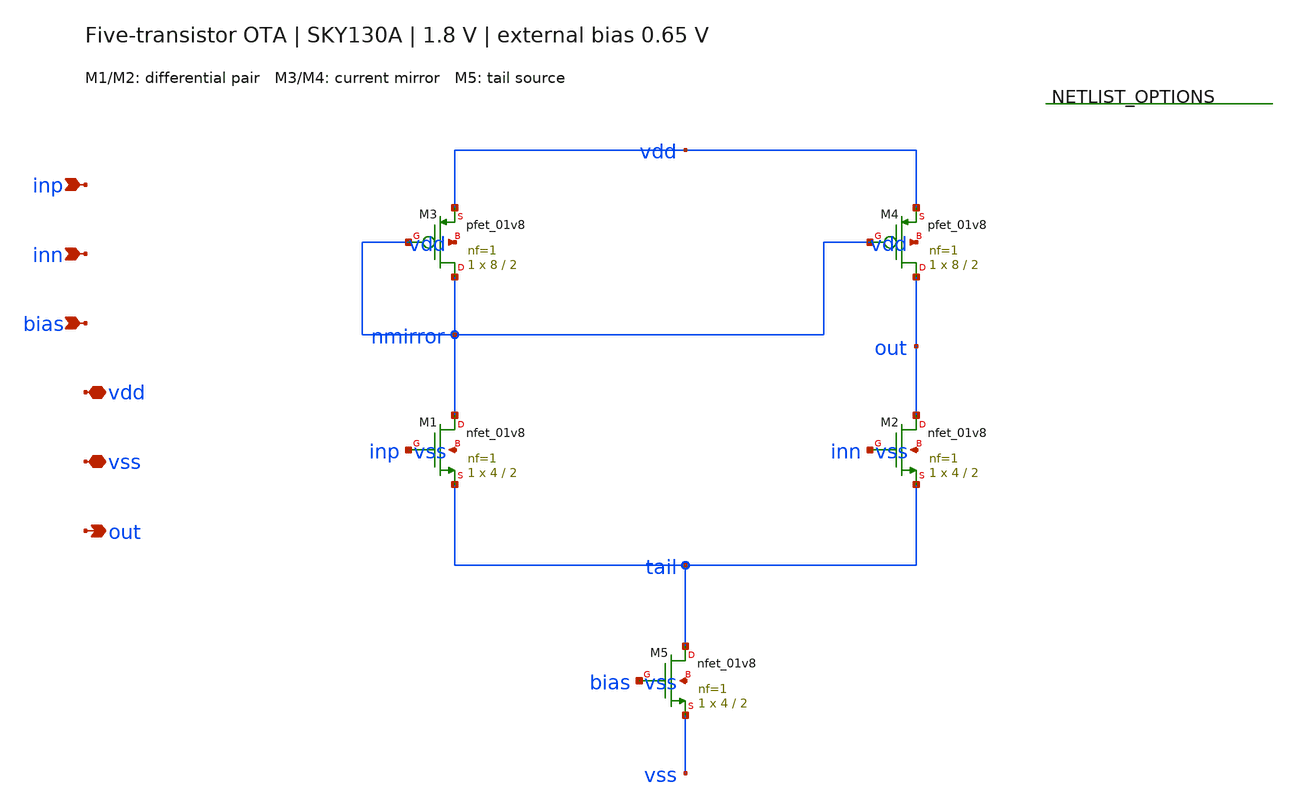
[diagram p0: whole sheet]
** sch_path: examples/ota5/schematics/ota5.sch
**.subckt ota5 inp inn bias vdd vss out
*.ipin inp
*.ipin inn
*.ipin bias
*.iopin vdd
*.iopin vss
*.opin out
XM1 nmirror inp tail vss sky130_fd_pr__nfet_01v8 L=2 W=4 nf=1 ad='int((1 + 1)/2) * 4 / 1 * 0.29' as='int((1 + 2)/2) * 4 / 1 * 0.29'
+ pd='2*int((1 + 1)/2) * (4 / 1 + 0.29)' ps='2*int((1 + 2)/2) * (4 / 1 + 0.29)' nrd='0.29 / 4 ' nrs='0.29 / 4 '
+ sa=0 sb=0 sd=0 mult=1 m=1
XM2 out inn tail vss sky130_fd_pr__nfet_01v8 L=2 W=4 nf=1 ad='int((1 + 1)/2) * 4 / 1 * 0.29' as='int((1 + 2)/2) * 4 / 1 * 0.29'
+ pd='2*int((1 + 1)/2) * (4 / 1 + 0.29)' ps='2*int((1 + 2)/2) * (4 / 1 + 0.29)' nrd='0.29 / 4 ' nrs='0.29 / 4 '
+ sa=0 sb=0 sd=0 mult=1 m=1
XM3 nmirror nmirror vdd vdd sky130_fd_pr__pfet_01v8 L=2 W=8 nf=1 ad='int((1 + 1)/2) * 8 / 1 * 0.29' as='int((1 + 2)/2) * 8 / 1 * 0.29'
+ pd='2*int((1 + 1)/2) * (8 / 1 + 0.29)' ps='2*int((1 + 2)/2) * (8 / 1 + 0.29)' nrd='0.29 / 8 ' nrs='0.29 / 8 '
+ sa=0 sb=0 sd=0 mult=1 m=1
XM4 out nmirror vdd vdd sky130_fd_pr__pfet_01v8 L=2 W=8 nf=1 ad='int((1 + 1)/2) * 8 / 1 * 0.29' as='int((1 + 2)/2) * 8 / 1 * 0.29'
+ pd='2*int((1 + 1)/2) * (8 / 1 + 0.29)' ps='2*int((1 + 2)/2) * (8 / 1 + 0.29)' nrd='0.29 / 8 ' nrs='0.29 / 8 '
+ sa=0 sb=0 sd=0 mult=1 m=1
XM5 tail bias vss vss sky130_fd_pr__nfet_01v8 L=2 W=4 nf=1 ad='int((1 + 1)/2) * 4 / 1 * 0.29' as='int((1 + 2)/2) * 4 / 1 * 0.29'
+ pd='2*int((1 + 1)/2) * (4 / 1 + 0.29)' ps='2*int((1 + 2)/2) * (4 / 1 + 0.29)' nrd='0.29 / 4 ' nrs='0.29 / 4 '
+ sa=0 sb=0 sd=0 mult=1 m=1
**.ends
.end
